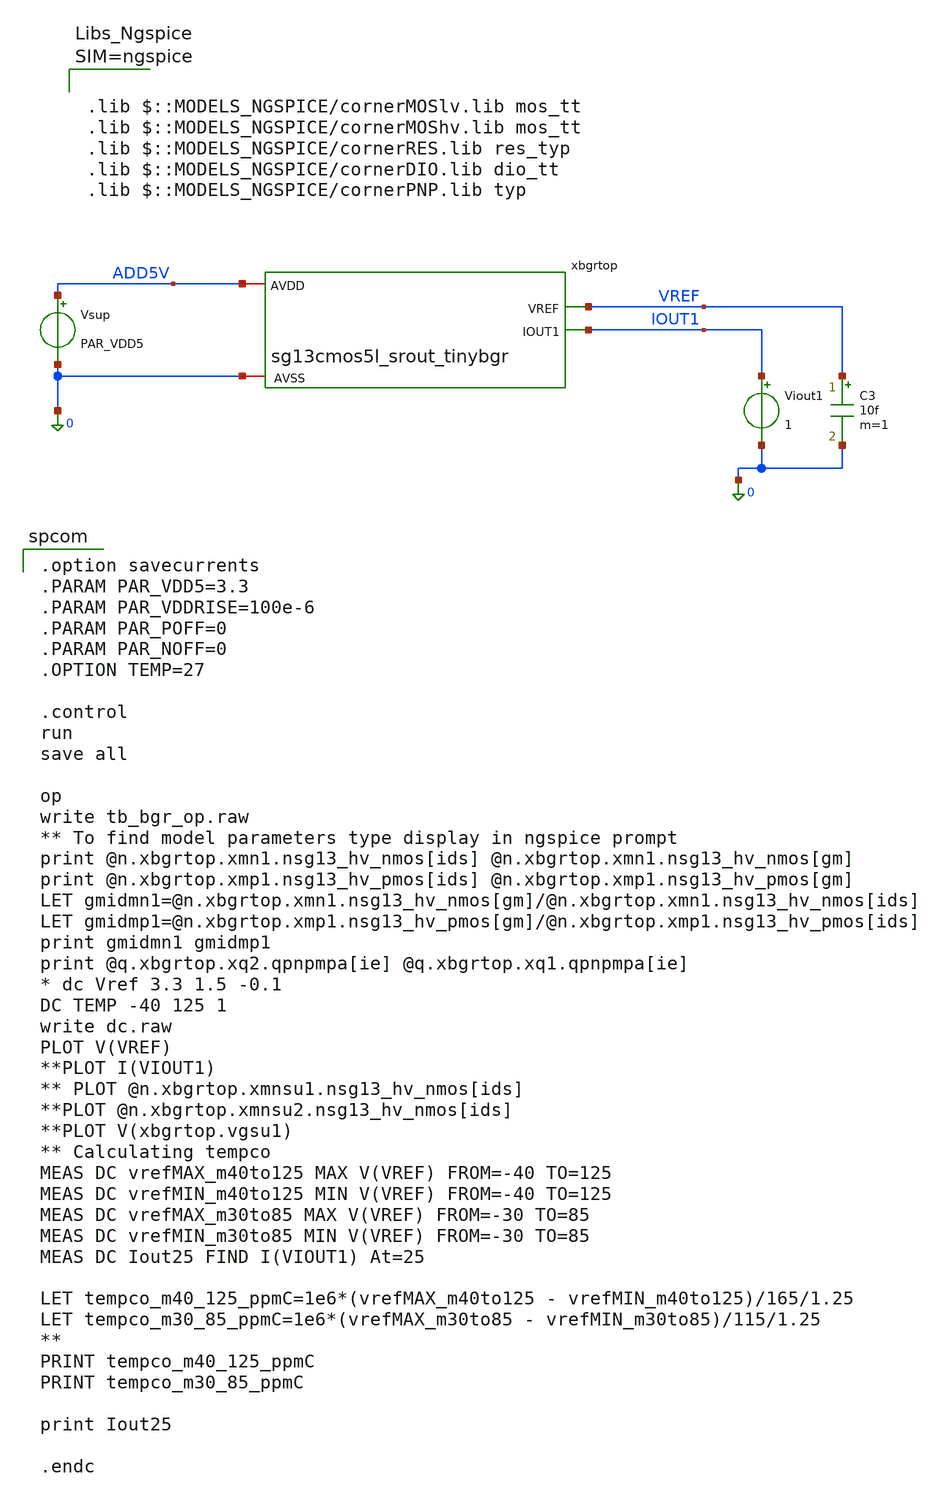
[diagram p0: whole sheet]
** sch_path: xschem/TB_tinybgr.sch
**.subckt TB_tinybgr
Vsup ADD5V 0 PAR_VDD5
C3 VREF 0 10f m=1
Viout1 IOUT1 0 1
xbgrtop ADD5V VREF IOUT1 0 sg13cmos5l_srout_tinybgr
**** begin user architecture code

.option savecurrents
.PARAM PAR_VDD5=3.3
.PARAM PAR_VDDRISE=100e-6
.PARAM PAR_POFF=0
.PARAM PAR_NOFF=0
.OPTION TEMP=27

.control
run
save all

op
write tb_bgr_op.raw
** To find model parameters type display in ngspice prompt
print @n.xbgrtop.xmn1.nsg13_hv_nmos[ids] @n.xbgrtop.xmn1.nsg13_hv_nmos[gm]
print @n.xbgrtop.xmp1.nsg13_hv_pmos[ids] @n.xbgrtop.xmp1.nsg13_hv_pmos[gm]
LET gmidmn1=@n.xbgrtop.xmn1.nsg13_hv_nmos[gm]/@n.xbgrtop.xmn1.nsg13_hv_nmos[ids]
LET gmidmp1=@n.xbgrtop.xmp1.nsg13_hv_pmos[gm]/@n.xbgrtop.xmp1.nsg13_hv_pmos[ids]
print gmidmn1 gmidmp1
print @q.xbgrtop.xq2.qpnpmpa[ie] @q.xbgrtop.xq1.qpnpmpa[ie]
* dc Vref 3.3 1.5 -0.1
DC TEMP -40 125 1
write dc.raw
PLOT V(VREF)
**PLOT I(VIOUT1)
** PLOT @n.xbgrtop.xmnsu1.nsg13_hv_nmos[ids]
**PLOT @n.xbgrtop.xmnsu2.nsg13_hv_nmos[ids]
**PLOT V(xbgrtop.vgsu1)
** Calculating tempco
MEAS DC vrefMAX_m40to125 MAX V(VREF) FROM=-40 TO=125
MEAS DC vrefMIN_m40to125 MIN V(VREF) FROM=-40 TO=125
MEAS DC vrefMAX_m30to85 MAX V(VREF) FROM=-30 TO=85
MEAS DC vrefMIN_m30to85 MIN V(VREF) FROM=-30 TO=85
MEAS DC Iout25 FIND I(VIOUT1) At=25

LET tempco_m40_125_ppmC=1e6*(vrefMAX_m40to125 - vrefMIN_m40to125)/165/1.25
LET tempco_m30_85_ppmC=1e6*(vrefMAX_m30to85 - vrefMIN_m30to85)/115/1.25
**
PRINT tempco_m40_125_ppmC
PRINT tempco_m30_85_ppmC

print Iout25

.endc




.lib $::MODELS_NGSPICE/cornerMOSlv.lib mos_tt
.lib $::MODELS_NGSPICE/cornerMOShv.lib mos_tt
.lib $::MODELS_NGSPICE/cornerRES.lib res_typ
.lib $::MODELS_NGSPICE/cornerDIO.lib dio_tt
.lib $::MODELS_NGSPICE/cornerPNP.lib typ




**** end user architecture code
**.ends

* expanding   symbol:  sg13cmos5l_srout_tinybgr.sym # of pins=4
** sym_path: xschem/sg13cmos5l_srout_tinybgr.sym
** sch_path: xschem/sg13cmos5l_srout_tinybgr.sch
.subckt sg13cmos5l_srout_tinybgr AVDD VREF IOUT1 AVSS
*.iopin AVDD
*.iopin AVSS
*.opin VREF
*.opin IOUT1
XQ1 AVSS AVSS Vbe1 pnpMPA a=2p p=6u m=8
XQ2 AVSS AVSS Vbe2 pnpMPA a=2p p=6u m=1
XMN2 Vgn Vgn Vbe2 AVSS sg13_hv_nmos w=2.6u l=1u ng=1 m=6 mm_ok=1
XMN1 Vgp Vgn Vbe2mr AVSS sg13_hv_nmos w=2.6u l=1u ng=1 m=12 mm_ok=1
XMP2 Vgn Vgp AVDD AVDD sg13_hv_pmos w=1u l=4u ng=1 m=3 mm_ok=1
XMP1 Vgp Vgp AVDD AVDD sg13_hv_pmos w=1u l=4u ng=1 m=6 mm_ok=1
XMP3 IOUT1 Vgp AVDD AVDD sg13_hv_pmos w=1u l=4u ng=1 m=11 mm_ok=1
XMP5 VREF Vgp AVDD AVDD sg13_hv_pmos w=1u l=4u ng=1 m=3 mm_ok=1
XMNSU1 AVDD vgsu1 Vgn AVSS sg13_hv_nmos w=1u l=2u ng=1 m=1 mm_ok=1
XMPSU1 net1 VREF AVDD AVDD sg13_hv_pmos w=0.35u l=6u ng=1 m=1 mm_ok=1
XMNSU2 vgsu1 VREF AVSS AVSS sg13_hv_nmos w=1u l=1u ng=1 m=1 mm_ok=1
XMPSU2 net2 VREF net1 AVDD sg13_hv_pmos w=0.35u l=6u ng=1 m=1 mm_ok=1
XMPSU3 net3 VREF net2 AVDD sg13_hv_pmos w=0.35u l=6u ng=1 m=1 mm_ok=1
XMPSU4 vgsu1 VREF net3 AVDD sg13_hv_pmos w=0.35u l=6u ng=1 m=1 mm_ok=1
xbgrres VREF Vbe2mr AVSS Vbe2 Vbe1 sg13cmos5l_srout_tinybgr_res
XQ3 AVSS AVSS AVSS pnpMPA a=2p p=6u m=2
XMN3 AVSS AVSS AVSS AVSS sg13_hv_nmos w=2.6u l=1u ng=1 m=2 mm_ok=1
XMN4 Vgn AVSS AVSS AVSS sg13_hv_nmos w=2.6u l=1u ng=1 m=2 mm_ok=1
XMN5 Vgp AVSS AVSS AVSS sg13_hv_nmos w=2.6u l=1u ng=1 m=4 mm_ok=1
XMP4 AVDD Vgp AVDD AVDD sg13_hv_pmos w=1u l=4u ng=1 m=4 mm_ok=1
XMP6 Vgn AVDD AVDD AVDD sg13_hv_pmos w=1u l=4u ng=1 m=1 mm_ok=1
XMP7 IOUT1 AVDD AVDD AVDD sg13_hv_pmos w=1u l=4u ng=1 m=1 mm_ok=1
XMP8 VREF AVDD AVDD AVDD sg13_hv_pmos w=1u l=4u ng=1 m=1 mm_ok=1
XMP9 AVDD AVDD AVDD AVDD sg13_hv_pmos w=1u l=4u ng=1 m=9 mm_ok=1
.ends


* expanding   symbol:  sg13cmos5l_srout_tinybgr_res.sym # of pins=5
** sym_path: xschem/sg13cmos5l_srout_tinybgr_res.sym
** sch_path: xschem/sg13cmos5l_srout_tinybgr_res.sch
.subckt sg13cmos5l_srout_tinybgr_res Vref Vbe2mr AVSS Vbe2 Vbe1
*.iopin Vbe1
*.iopin Vbe2
*.iopin AVSS
*.iopin Vbe2mr
*.iopin Vref
XR3 Vbe2mr net21 AVSS rhigh w=1.1u l=4u m=1 b=0 mm_ok=1
XR1 net21 Vbe1 AVSS rhigh w=1.1u l=4u m=1 b=0 mm_ok=1
XR2 net2 net1 AVSS rhigh w=1.1u l=4u m=1 b=0 mm_ok=1
XR4 net1 Vbe2 AVSS rhigh w=1.1u l=4u m=1 b=0 mm_ok=1
XR5 net3 net2 AVSS rhigh w=1.1u l=4u m=1 b=0 mm_ok=1
XR6 net4 net3 AVSS rhigh w=1.1u l=4u m=1 b=0 mm_ok=1
XR7 net22 net4 AVSS rhigh w=1.1u l=4u m=1 b=0 mm_ok=1
XR8 net6 net5 AVSS rhigh w=1.1u l=4u m=1 b=0 mm_ok=1
XR9 net5 net23 AVSS rhigh w=1.1u l=4u m=1 b=0 mm_ok=1
XR10 net7 net6 AVSS rhigh w=1.1u l=4u m=1 b=0 mm_ok=1
XR11 net8 net7 AVSS rhigh w=1.1u l=4u m=1 b=0 mm_ok=1
XR12 net22 net8 AVSS rhigh w=1.1u l=4u m=1 b=0 mm_ok=1
XR13 net10 net9 AVSS rhigh w=1.1u l=4u m=1 b=0 mm_ok=1
XR14 net9 net23 AVSS rhigh w=1.1u l=4u m=1 b=0 mm_ok=1
XR15 net11 net10 AVSS rhigh w=1.1u l=4u m=1 b=0 mm_ok=1
XR16 net12 net11 AVSS rhigh w=1.1u l=4u m=1 b=0 mm_ok=1
XR17 net24 net12 AVSS rhigh w=1.1u l=4u m=1 b=0 mm_ok=1
XR18 net14 net13 AVSS rhigh w=1.1u l=4u m=1 b=0 mm_ok=1
XR19 net13 net25 AVSS rhigh w=1.1u l=4u m=1 b=0 mm_ok=1
XR20 net15 net14 AVSS rhigh w=1.1u l=4u m=1 b=0 mm_ok=1
XR21 net16 net15 AVSS rhigh w=1.1u l=4u m=1 b=0 mm_ok=1
XR22 net24 net16 AVSS rhigh w=1.1u l=4u m=1 b=0 mm_ok=1
XR23 net18 net17 AVSS rhigh w=1.1u l=4u m=1 b=0 mm_ok=1
XR24 net17 net26 AVSS rhigh w=1.1u l=4u m=1 b=0 mm_ok=1
XR25 net19 net18 AVSS rhigh w=1.1u l=4u m=1 b=0 mm_ok=1
XR26 net20 net19 AVSS rhigh w=1.1u l=4u m=1 b=0 mm_ok=1
XR27 Vref net20 AVSS rhigh w=1.1u l=4u m=1 b=0 mm_ok=1
XR28 net25 net27 AVSS rhigh w=1.1u l=4u m=1 b=0 mm_ok=1
XR29 net26 net27 AVSS rhigh w=1.1u l=4u m=1 b=0 mm_ok=1
XR30 AVSS AVSS AVSS rhigh w=1.1u l=4u m=9 b=0 mm_ok=1
.ends

.end
